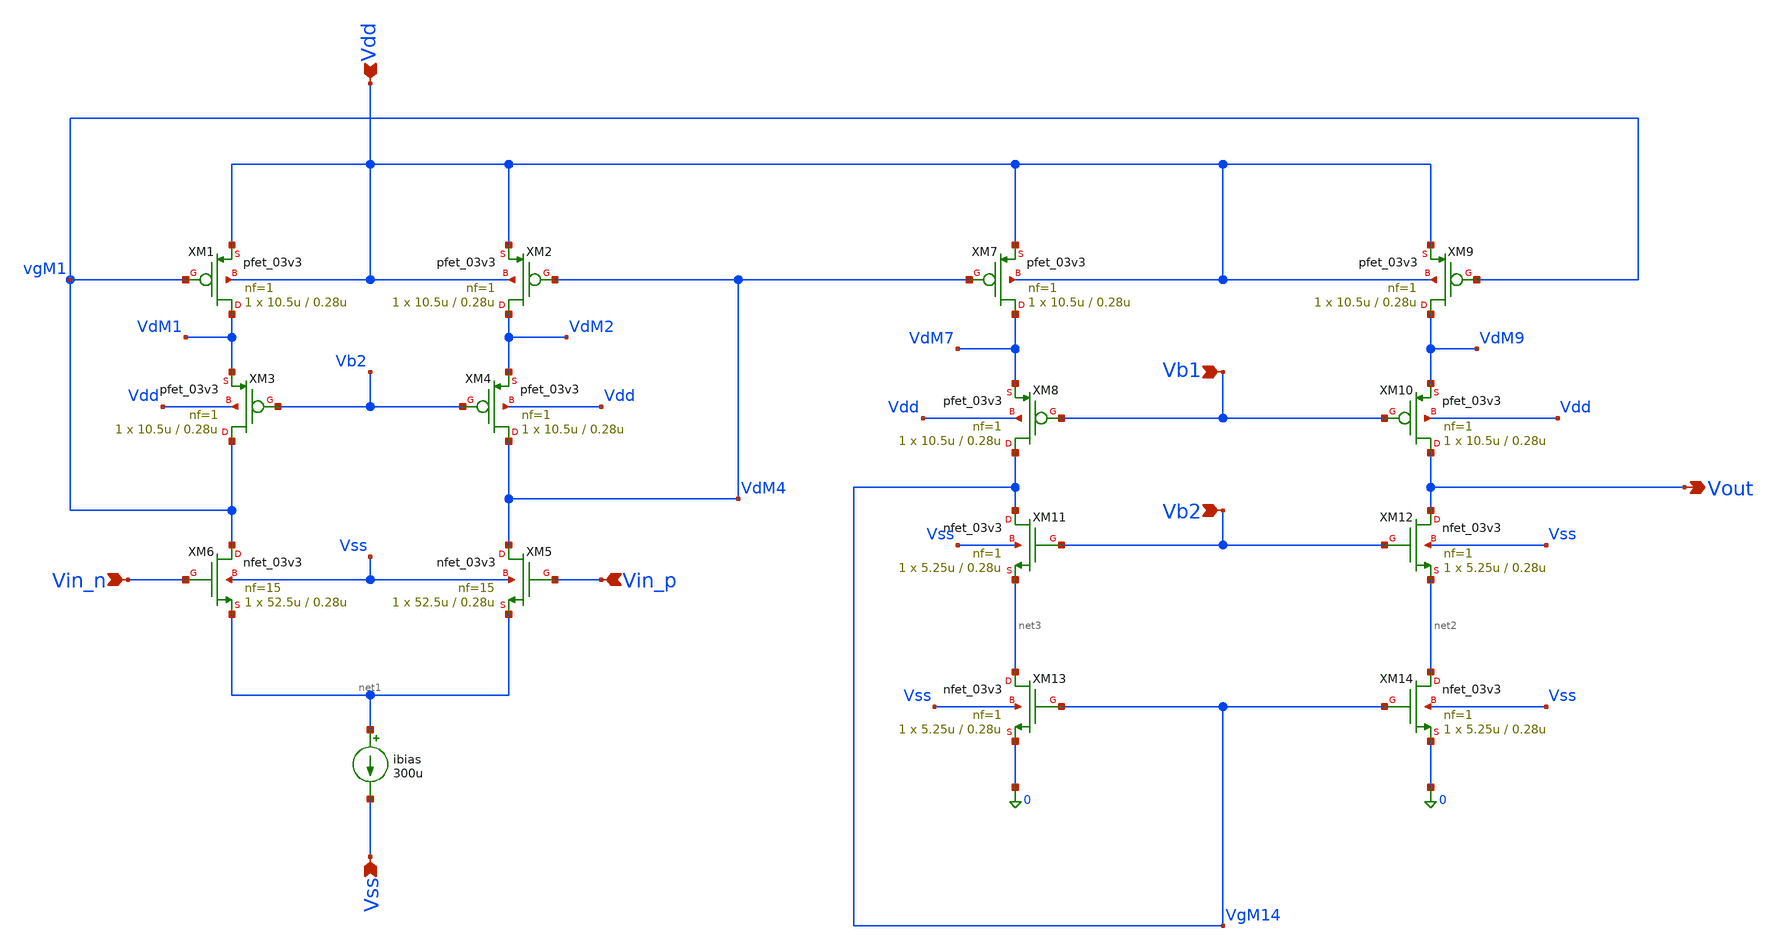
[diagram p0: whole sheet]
** sch_path: blocks/adc/lvds/op_amp.sch
**.subckt op_amp Vdd Vb2 Vin_p Vin_n Vb1 Vout Vss
*.ipin Vdd
*.ipin Vb2
*.ipin Vin_p
*.ipin Vin_n
*.ipin Vb1
*.opin Vout
*.ipin Vss
XM1 VdM1 vgM1 Vdd Vdd pfet_03v3 L=0.28u W=10.5u nf=1 ad='int((nf+1)/2) * W/nf * 0.18u' as='int((nf+2)/2) * W/nf * 0.18u'
+ pd='2*int((nf+1)/2) * (W/nf + 0.18u)' ps='2*int((nf+2)/2) * (W/nf + 0.18u)' nrd='0.18u / W' nrs='0.18u / W'
+ sa=0 sb=0 sd=0 m=1
XM2 VdM2 VdM4 Vdd Vdd pfet_03v3 L=0.28u W=10.5u nf=1 ad='int((nf+1)/2) * W/nf * 0.18u' as='int((nf+2)/2) * W/nf * 0.18u'
+ pd='2*int((nf+1)/2) * (W/nf + 0.18u)' ps='2*int((nf+2)/2) * (W/nf + 0.18u)' nrd='0.18u / W' nrs='0.18u / W'
+ sa=0 sb=0 sd=0 m=1
XM3 vgM1 Vb2 VdM1 Vdd pfet_03v3 L=0.28u W=10.5u nf=1 ad='int((nf+1)/2) * W/nf * 0.18u' as='int((nf+2)/2) * W/nf * 0.18u'
+ pd='2*int((nf+1)/2) * (W/nf + 0.18u)' ps='2*int((nf+2)/2) * (W/nf + 0.18u)' nrd='0.18u / W' nrs='0.18u / W'
+ sa=0 sb=0 sd=0 m=1
XM4 VdM4 Vb2 VdM2 Vdd pfet_03v3 L=0.28u W=10.5u nf=1 ad='int((nf+1)/2) * W/nf * 0.18u' as='int((nf+2)/2) * W/nf * 0.18u'
+ pd='2*int((nf+1)/2) * (W/nf + 0.18u)' ps='2*int((nf+2)/2) * (W/nf + 0.18u)' nrd='0.18u / W' nrs='0.18u / W'
+ sa=0 sb=0 sd=0 m=1
XM5 VdM4 Vin_p net1 Vss nfet_03v3 L=0.28u W=52.5u nf=15 ad='int((nf+1)/2) * W/nf * 0.18u' as='int((nf+2)/2) * W/nf * 0.18u'
+ pd='2*int((nf+1)/2) * (W/nf + 0.18u)' ps='2*int((nf+2)/2) * (W/nf + 0.18u)' nrd='0.18u / W' nrs='0.18u / W'
+ sa=0 sb=0 sd=0 m=1
XM6 vgM1 Vin_n net1 Vss nfet_03v3 L=0.28u W=52.5u nf=15 ad='int((nf+1)/2) * W/nf * 0.18u' as='int((nf+2)/2) * W/nf * 0.18u'
+ pd='2*int((nf+1)/2) * (W/nf + 0.18u)' ps='2*int((nf+2)/2) * (W/nf + 0.18u)' nrd='0.18u / W' nrs='0.18u / W'
+ sa=0 sb=0 sd=0 m=1
XM7 VdM7 VdM4 Vdd Vdd pfet_03v3 L=0.28u W=10.5u nf=1 ad='int((nf+1)/2) * W/nf * 0.18u' as='int((nf+2)/2) * W/nf * 0.18u'
+ pd='2*int((nf+1)/2) * (W/nf + 0.18u)' ps='2*int((nf+2)/2) * (W/nf + 0.18u)' nrd='0.18u / W' nrs='0.18u / W'
+ sa=0 sb=0 sd=0 m=1
XM9 VdM9 vgM1 Vdd Vdd pfet_03v3 L=0.28u W=10.5u nf=1 ad='int((nf+1)/2) * W/nf * 0.18u' as='int((nf+2)/2) * W/nf * 0.18u'
+ pd='2*int((nf+1)/2) * (W/nf + 0.18u)' ps='2*int((nf+2)/2) * (W/nf + 0.18u)' nrd='0.18u / W' nrs='0.18u / W'
+ sa=0 sb=0 sd=0 m=1
XM11 VgM14 Vb2 net3 Vss nfet_03v3 L=0.28u W=5.25u nf=1 ad='int((nf+1)/2) * W/nf * 0.18u' as='int((nf+2)/2) * W/nf * 0.18u'
+ pd='2*int((nf+1)/2) * (W/nf + 0.18u)' ps='2*int((nf+2)/2) * (W/nf + 0.18u)' nrd='0.18u / W' nrs='0.18u / W'
+ sa=0 sb=0 sd=0 m=1
XM12 Vout Vb2 net2 Vss nfet_03v3 L=0.28u W=5.25u nf=1 ad='int((nf+1)/2) * W/nf * 0.18u' as='int((nf+2)/2) * W/nf * 0.18u'
+ pd='2*int((nf+1)/2) * (W/nf + 0.18u)' ps='2*int((nf+2)/2) * (W/nf + 0.18u)' nrd='0.18u / W' nrs='0.18u / W'
+ sa=0 sb=0 sd=0 m=1
XM13 net3 VgM14 0 Vss nfet_03v3 L=0.28u W=5.25u nf=1 ad='int((nf+1)/2) * W/nf * 0.18u' as='int((nf+2)/2) * W/nf * 0.18u'
+ pd='2*int((nf+1)/2) * (W/nf + 0.18u)' ps='2*int((nf+2)/2) * (W/nf + 0.18u)' nrd='0.18u / W' nrs='0.18u / W'
+ sa=0 sb=0 sd=0 m=1
XM14 net2 VgM14 0 Vss nfet_03v3 L=0.28u W=5.25u nf=1 ad='int((nf+1)/2) * W/nf * 0.18u' as='int((nf+2)/2) * W/nf * 0.18u'
+ pd='2*int((nf+1)/2) * (W/nf + 0.18u)' ps='2*int((nf+2)/2) * (W/nf + 0.18u)' nrd='0.18u / W' nrs='0.18u / W'
+ sa=0 sb=0 sd=0 m=1
XM8 VgM14 Vb1 VdM7 Vdd pfet_03v3 L=0.28u W=10.5u nf=1 ad='int((nf+1)/2) * W/nf * 0.18u' as='int((nf+2)/2) * W/nf * 0.18u'
+ pd='2*int((nf+1)/2) * (W/nf + 0.18u)' ps='2*int((nf+2)/2) * (W/nf + 0.18u)' nrd='0.18u / W' nrs='0.18u / W'
+ sa=0 sb=0 sd=0 m=1
XM10 Vout Vb1 VdM9 Vdd pfet_03v3 L=0.28u W=10.5u nf=1 ad='int((nf+1)/2) * W/nf * 0.18u' as='int((nf+2)/2) * W/nf * 0.18u'
+ pd='2*int((nf+1)/2) * (W/nf + 0.18u)' ps='2*int((nf+2)/2) * (W/nf + 0.18u)' nrd='0.18u / W' nrs='0.18u / W'
+ sa=0 sb=0 sd=0 m=1
ibias net1 Vss 300u
**.ends
.end
